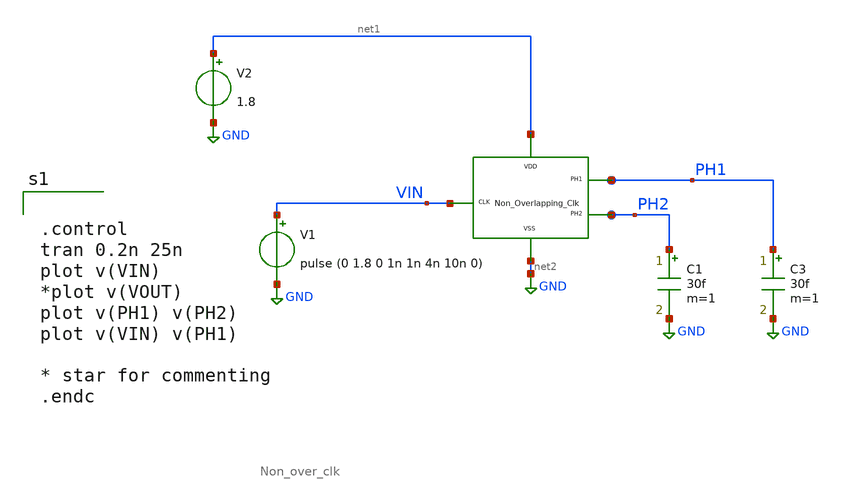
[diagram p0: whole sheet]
** sch_path: xschem/DC_DC_Converter_xschem/OTHERS/DC_DC_Converter_JV9/Non_Overlap_Clk/Non_over_clk_TB.sch
**.subckt Non_over_clk_TB
V1 VIN GND pulse (0 1.8 0 1n 1n 4n 10n 0)
V2 net1 GND 1.8
C3 PH1 GND 30f m=1
C1 PH2 GND 30f m=1
x1 net1 VIN PH1 net2 PH2 Non_over_clk
**** begin user architecture code


.control
tran 0.2n 25n
plot v(VIN)
*plot v(VOUT)
plot v(PH1) v(PH2)
plot v(VIN) v(PH1)

* star for commenting
.endc


** opencircuitdesign pdks install
.lib $::SKYWATER_MODELS/sky130.lib.spice tt


**** end user architecture code
**.ends
.GLOBAL GND
.end
